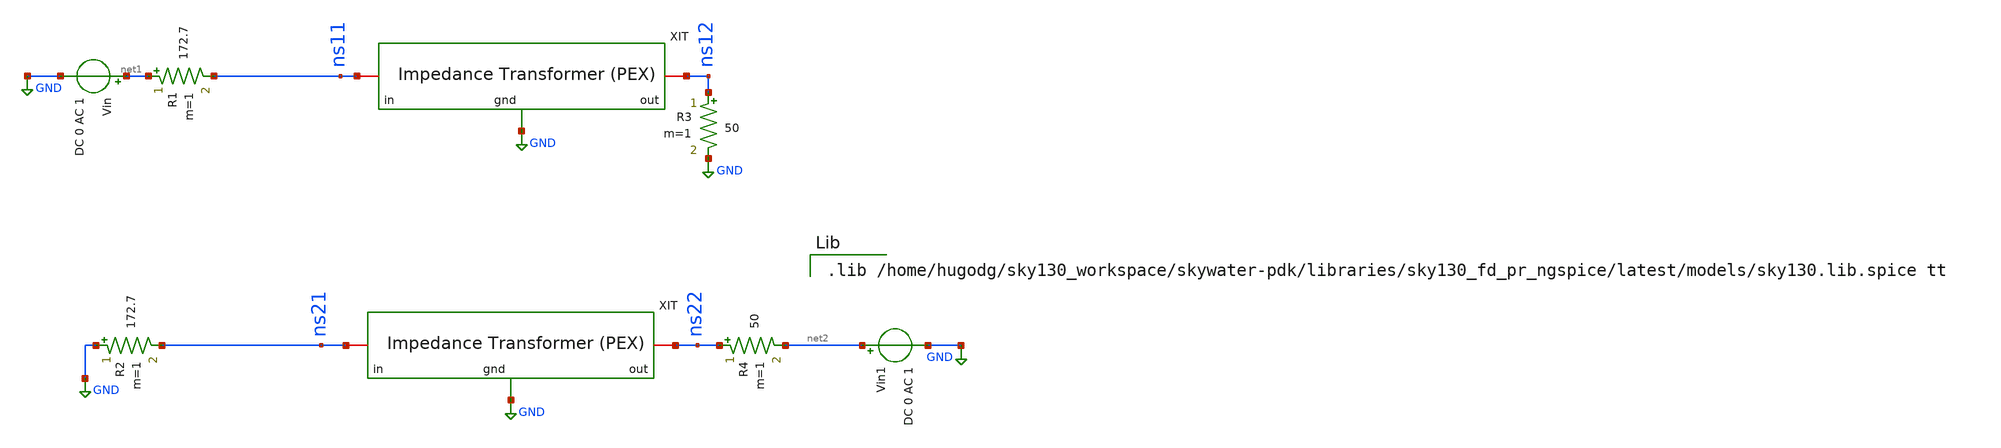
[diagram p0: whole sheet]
** sch_path: impedance-transformer/xschem/impedance-transformer-pex_tb-ac.sch
**.subckt impedance-transformer-pex_tb-ac
Vin net1 GND DC 0 AC 1
Vin1 net2 GND DC 0 AC 1
R3 ns12 GND 50 m=1
R4 ns22 net2 50 m=1
xit1 ns11 ns12 GND impedance-transformer-pex
xit2 ns21 ns22 GND impedance-transformer-pex
R1 net1 ns11 172.7 m=1
R2 GND ns21 172.7 m=1
**** begin user architecture code



.ac lin 1MEG 1.5G 4G
.control
destroy all
set units=degrees
run

set color0=white
set color1=black

let z0=50
let zl=169

* Find two S parameters from test circuit
let s11 = v(ns11)
let s12 = v(ns12)
let s21 = v(ns21)
let s22 = v(ns22)

* Extract Y parameters
*let StoYDelS = ((1+s11)*(1+s22)-s12*s21)*z0
*let y11 = ((1+s22)*(1-s11)+s12*s21/StoYDelS
*let y12=-2*s12/StoYDelS
*let y21=-2*s21/StoYDelS
*let y22 = ((1+s11)*(1-s22)+s12+s21)/StoYDelS

* Extract Z parameters
let StoZDelS = ((1-s11)*(1-s22)-s12*s21)/z0
let z11 = ((1+s11)*(1-s22)+s12*s21)/StoZDelS
let z12 = 2*s12/StoZDelS
let z21 = 2*s21/StoZDelS
let z22=((1-s11)*(1+s22)+s12*s21)/StoZDelS

*plot z11
*plot z12
*plot z21
*plot z22 xlimit 2.4G 2.5G
*plot ph(z22) xlimit 2.4G 2.5G
*plot z22
*plot smith z22
let z_in =z11-z12*z21/(z22+z0)
plot ph(z_in)
plot mag(z_in)
let z_output=z22-(z12*z21/(z11+zl))
plot ph(z_output)
plot mag(z_output)
let gamma=(mag(z_output)-mag(z_in))/(mag(z_output)+mag(z_in))
plot gamma*100
.endc


.lib /home/hugodg/sky130_workspace/skywater-pdk/libraries/sky130_fd_pr_ngspice/latest/models/sky130.lib.spice tt

**** end user architecture code
**.ends

* expanding   symbol:
*+  /home/hugodg/projects_sky130/temp_sensor/impedance-transformer/xschem/impedance-transformer-pex.sym # of pins=3
** sym_path: impedance-transformer/xschem/impedance-transformer-pex.sym
** sch_path: impedance-transformer/xschem/impedance-transformer-pex.sch
.subckt impedance-transformer-pex in out gnd
*.iopin gnd
*.iopin in
*.iopin out
xl1 in out l1
**** begin user architecture code

* NGSPICE file created from impedance-transformer.ext - technology: sky130A

.subckt sky130_fd_pr__cap_mim_m3_2_3YFQRG m4_n2675_n10534# c2_n2575_n10434# VSUBS
X0 c2_n2575_n10434# m4_n2675_n10534# sky130_fd_pr__cap_mim_m3_2 l=2.496e+07u w=2.496e+07u
X1 c2_n2575_n10434# m4_n2675_n10534# sky130_fd_pr__cap_mim_m3_2 l=2.496e+07u w=2.496e+07u
X2 c2_n2575_n10434# m4_n2675_n10534# sky130_fd_pr__cap_mim_m3_2 l=2.496e+07u w=2.496e+07u
X3 c2_n2575_n10434# m4_n2675_n10534# sky130_fd_pr__cap_mim_m3_2 l=2.496e+07u w=2.496e+07u
C0 c2_n2575_n10434# m4_n2675_n10534# 164.66fF
C1 c2_n2575_n10434# VSUBS 0.30fF
C2 m4_n2675_n10534# VSUBS 42.24fF
.ends

.subckt sky130_fd_pr__cap_mim_m3_2_93FFAE c2_n2522_n7629# m4_n2622_n7729# VSUBS
X0 c2_n2522_n7629# m4_n2622_n7729# sky130_fd_pr__cap_mim_m3_2 l=2.443e+07u w=2.443e+07u
X1 c2_n2522_n7629# m4_n2622_n7729# sky130_fd_pr__cap_mim_m3_2 l=2.443e+07u w=2.443e+07u
X2 c2_n2522_n7629# m4_n2622_n7729# sky130_fd_pr__cap_mim_m3_2 l=2.443e+07u w=2.443e+07u
C0 c2_n2522_n7629# m4_n2622_n7729# 118.74fF
C1 c2_n2522_n7629# VSUBS 0.26fF
C2 m4_n2622_n7729# VSUBS 30.75fF
.ends

*.subckt impedance-transformer gnd out in
Xsky130_fd_pr__cap_mim_m3_2_3YFQRG_0 gnd out gnd sky130_fd_pr__cap_mim_m3_2_3YFQRG
Xsky130_fd_pr__cap_mim_m3_2_3YFQRG_1 gnd out gnd sky130_fd_pr__cap_mim_m3_2_3YFQRG
Xsky130_fd_pr__cap_mim_m3_2_3YFQRG_2 gnd out gnd sky130_fd_pr__cap_mim_m3_2_3YFQRG
Xsky130_fd_pr__cap_mim_m3_2_3YFQRG_3 gnd out gnd sky130_fd_pr__cap_mim_m3_2_3YFQRG
Xsky130_fd_pr__cap_mim_m3_2_93FFAE_0 in gnd gnd sky130_fd_pr__cap_mim_m3_2_93FFAE
Xsky130_fd_pr__cap_mim_m3_2_93FFAE_1 in gnd gnd sky130_fd_pr__cap_mim_m3_2_93FFAE
Xsky130_fd_pr__cap_mim_m3_2_93FFAE_2 in gnd gnd sky130_fd_pr__cap_mim_m3_2_93FFAE

R0 out out.n2 0.192
R1 out.t15 out.t13 0.066
R2 out.t14 out.t15 0.066
R3 out.t12 out.t14 0.066
R4 out.t11 out.t9 0.066
R5 out.t10 out.t11 0.066
R6 out.t8 out.t10 0.066
R7 out.t7 out.t5 0.066
R8 out.t6 out.t7 0.066
R9 out.t4 out.t6 0.066
R10 out.t3 out.t1 0.066
R11 out.t2 out.t3 0.066
R12 out.t0 out.t2 0.066
R13 out.n1 out.t0 0.062
R14 out.n0 out.t12 0.056
R15 out.n1 out.t4 0.047
R16 out.n0 out.t8 0.046
R17 out.n2 out.n1 0.006
R18 out.n2 out.n0 0.004
R19 in in.n0 0.26
R20 in.t2 in.t0 0.066
R21 in.t1 in.t2 0.066
R22 in.t5 in.t3 0.066
R23 in.t4 in.t5 0.066
R24 in.t8 in.t6 0.066
R25 in.t7 in.t8 0.064
R26 in.n0 in.t1 0.05
R27 in.n0 in.t7 0.047
R28 in.n0 in.t4 0.039
C0 in.t6 gnd 14.51fF
C1 in.t8 gnd 14.50fF
C2 in.t7 gnd 37.65fF
C3 in.t3 gnd 14.51fF
C4 in.t5 gnd 14.54fF
C5 in.t4 gnd 14.38fF
C6 in.t0 gnd 14.51fF
C7 in.t2 gnd 14.54fF
C8 in.t1 gnd 20.60fF
C9 in.n0 gnd 474.44fF $ **FLOATING
C10 out.t9 gnd 17.89fF
C11 out.t11 gnd 17.93fF
C12 out.t10 gnd 17.93fF
C13 out.t8 gnd 18.23fF
C14 out.t13 gnd 17.89fF
C15 out.t15 gnd 17.93fF
C16 out.t14 gnd 17.93fF
C17 out.t12 gnd 24.02fF
C18 out.n0 gnd 54.72fF $ **FLOATING
C19 out.t5 gnd 17.89fF
C20 out.t7 gnd 17.93fF
C21 out.t6 gnd 17.93fF
C22 out.t4 gnd 18.28fF
C23 out.t1 gnd 17.89fF
C24 out.t3 gnd 17.93fF
C25 out.t2 gnd 17.93fF
C26 out.t0 gnd 22.51fF
C27 out.n1 gnd 54.23fF $ **FLOATING
C28 out.n2 gnd 512.64fF $ **FLOATING
C29 in gnd 311.92fF
C30 out gnd 306.12fF
*.ends



**** end user architecture code
.ends


* expanding   symbol:  /home/hugodg/projects_sky130/temp_sensor/impedance-transformer/xschem/l1.sym
*+ # of pins=2
** sym_path: impedance-transformer/xschem/l1.sym
** sch_path: impedance-transformer/xschem/l1.sch
.subckt l1 p1 p2
*.iopin p2
*.iopin p1
L0 p1 net3 592.7p m=1
Cs1 p1 net1 26.83f m=1
Cs2 p2 net2 24.25f m=1
Rs1 net1 GND 65.02 m=1
Rs2 net2 GND 14.4 m=1
R1 p2 net3 2.935 m=1
.ends

.GLOBAL GND
.end
